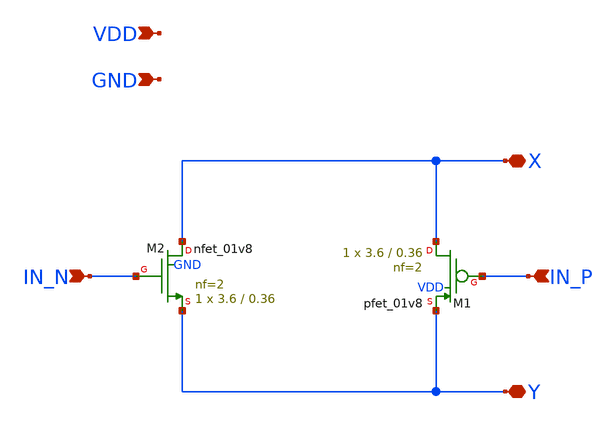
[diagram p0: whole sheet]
** sch_path: swtch_switch_sky130nm/design/SWTCH_SWITCH_SKY130NM/SWTCH_SWITCH.sch
**.subckt SWTCH_SWITCH IN_N Y IN_P X VDD GND
*.ipin IN_N
*.iopin Y
*.ipin IN_P
*.iopin X
*.ipin VDD
*.ipin GND
XM1 X IN_P Y VDD sky130_fd_pr__pfet_01v8 L=0.36 W=3.6 nf=2 ad='int((nf+1)/2) * W/nf * 0.29' as='int((nf+2)/2) * W/nf * 0.29'
+ pd='2*int((nf+1)/2) * (W/nf + 0.29)' ps='2*int((nf+2)/2) * (W/nf + 0.29)' nrd='0.29 / W' nrs='0.29 / W'
+ sa=0 sb=0 sd=0 mult=1 m=1
XM2 X IN_N Y GND sky130_fd_pr__nfet_01v8 L=0.36 W=3.6 nf=2 ad='int((nf+1)/2) * W/nf * 0.29' as='int((nf+2)/2) * W/nf * 0.29'
+ pd='2*int((nf+1)/2) * (W/nf + 0.29)' ps='2*int((nf+2)/2) * (W/nf + 0.29)' nrd='0.29 / W' nrs='0.29 / W'
+ sa=0 sb=0 sd=0 mult=1 m=1
**.ends
.end
